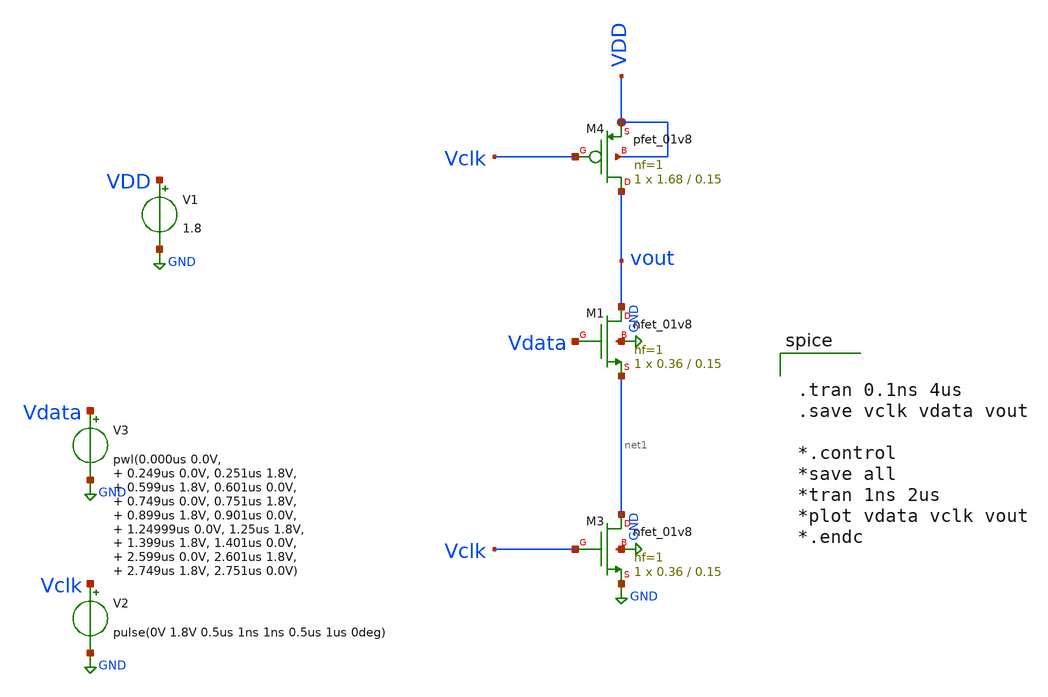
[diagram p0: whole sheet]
** sch_path: TSPC_Dff_secStage.sch
**.subckt TSPC_Dff_secStage
V1 VDD GND 1.8
V2 Vclk GND pulse(0V 1.8V 0.5us 1ns 1ns 0.5us 1us 0deg)
V3 Vdata GND pwl(0.000us 0.0V, 0.249us 0.0V, 0.251us 1.8V, 0.599us 1.8V, 0.601us 0.0V, 0.749us 0.0V,
+ 0.751us 1.8V, 0.899us 1.8V, 0.901us 0.0V, 1.24999us 0.0V, 1.25us 1.8V, 1.399us 1.8V, 1.401us 0.0V, 2.599us
+ 0.0V, 2.601us 1.8V, 2.749us 1.8V, 2.751us 0.0V)
XM3 net1 Vclk GND GND sky130_fd_pr__nfet_01v8 L=0.15 W=0.36 nf=1 ad='int((nf+1)/2) * W/nf * 0.29' as='int((nf+2)/2) * W/nf * 0.29'
+ pd='2*int((nf+1)/2) * (W/nf + 0.29)' ps='2*int((nf+2)/2) * (W/nf + 0.29)' nrd='0.29 / W' nrs='0.29 / W'
+ sa=0 sb=0 sd=0 mult=1 m=1
XM4 vout Vclk VDD VDD sky130_fd_pr__pfet_01v8 L=0.15 W=1.68 nf=1 ad='int((nf+1)/2) * W/nf * 0.29' as='int((nf+2)/2) * W/nf * 0.29'
+ pd='2*int((nf+1)/2) * (W/nf + 0.29)' ps='2*int((nf+2)/2) * (W/nf + 0.29)' nrd='0.29 / W' nrs='0.29 / W'
+ sa=0 sb=0 sd=0 mult=1 m=1
XM1 vout Vdata net1 GND sky130_fd_pr__nfet_01v8 L=0.15 W=0.36 nf=1 ad='int((nf+1)/2) * W/nf * 0.29' as='int((nf+2)/2) * W/nf * 0.29'
+ pd='2*int((nf+1)/2) * (W/nf + 0.29)' ps='2*int((nf+2)/2) * (W/nf + 0.29)' nrd='0.29 / W' nrs='0.29 / W'
+ sa=0 sb=0 sd=0 mult=1 m=1
**** begin user architecture code


.tran 0.1ns 4us
.save vclk vdata vout

*.control
*save all
*tran 1ns 2us
*plot vdata vclk vout
*.endc



*.lib ~/open_pdks/sky130/sky130A/libs.tech/ngspice/sky130.lib.spice tt
.param mc_mm_switch=0
.param mc_pr_switch=0

.include ~/open_pdks/sky130/sky130A/libs.tech/ngspice/corners/tt/nonfet.spice


*model
.include ~/open_pdks/sky130/sky130A/libs.tech/ngspice/all.spice

*mosfet
.include ~/open_pdks/sky130/sky130A/libs.ref/sky130_fd_pr/spice/sky130_fd_pr__pfet_01v8__tt.corner.spice
.inclued ~/open_pdks/sky130/sky130A/libs.ref/sky130_fd_pr/spice/sky130_fd_pr__nfet_01v8__tt.corner.spice

*mismatch parameters
.include ~/open_pdks/sky130/sky130A/libs.ref/sky130_fd_pr/spice/sky130_fd_pr__pfet_01v8__mismatch.corner.spice
.include ~/open_pdks/sky130/sky130A/libs.ref/sky130_fd_pr/spice/sky130_fd_pr__nfet_01v8__mismatch.corner.spice

**** end user architecture code
**.ends
.GLOBAL GND
.end
